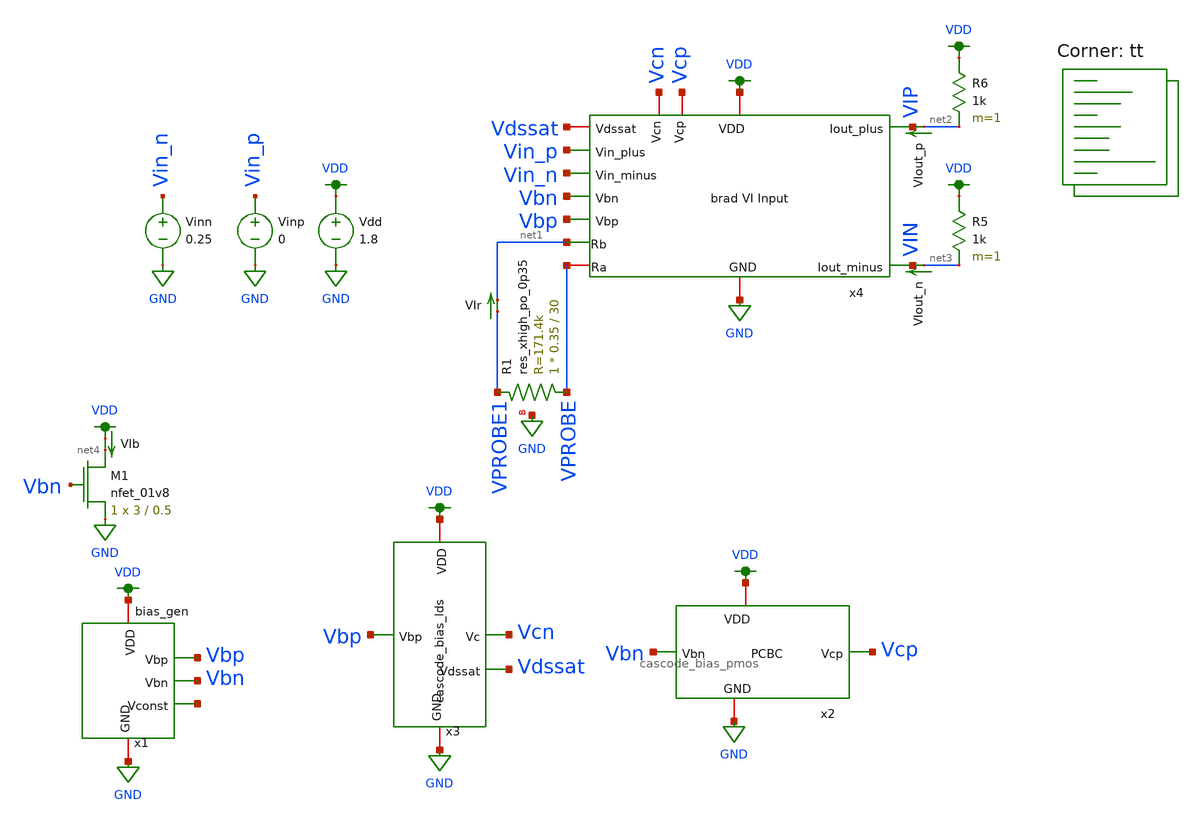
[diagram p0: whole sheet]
** sch_path: final/schematics/brad_VI_input_tb.sch
**.subckt brad_VI_input_tb
Vdd VDD GND 1.8
Vinp Vin_p GND 0
Vinn Vin_n GND 0.25
XM1 net4 Vbn GND GND sky130_fd_pr__nfet_01v8 L=0.5 W=3 nf=1 ad='int((nf+1)/2) * W/nf * 0.29' as='int((nf+2)/2) * W/nf * 0.29'
+ pd='2*int((nf+1)/2) * (W/nf + 0.29)' ps='2*int((nf+2)/2) * (W/nf + 0.29)' nrd='0.29 / W' nrs='0.29 / W'
+ sa=0 sb=0 sd=0 mult=1 m=1
VIb VDD net4 0
.save i(vib)
x3 Vbp VDD Vcn GND Vdssat cascode_bias_lds
x4 VDD VIP VIN Vin_p Vin_n Vbn Vbp Vcn GND VPROBE net1 Vdssat Vcp brad_VI_input
VIr VPROBE1 net1 0
.save i(vir)
VIout_p net2 VIP 0
.save i(viout_p)
VIout_n net3 VIN 0
.save i(viout_n)
R5 VDD net3 1k m=1
R6 VDD net2 1k m=1
x1 VDD Vbp net5 GND Vbn bias_gen
XR1 VPROBE VPROBE1 GND sky130_fd_pr__res_xhigh_po_0p35 L=30 mult=1 m=1
x2 Vbn VDD GND Vcp cascode_bias_pmos
**** begin user architecture code


.control
  save all
  set wr_vecnames
  set wr_singlescale
  remzerovec
  * tran 1u 100m
  dc Vinp 0 1.8 0.01
  write brad_VI_input_tb.raw
  wrdata ~/Documents/madvlsi/final/schematics/brad_VI_input.txt v(vin_p) i(v.x4.vib) i(v.x4.vibx2)
+ v(x4.min1) v(x4.min2) i(vir) i(viout_p) i(viout_n)
  quit
.endc


.lib $::SKYWATER_MODELS/sky130.lib.spice tt
**** end user architecture code
**.ends
.GLOBAL GND
.GLOBAL VDD
.end
